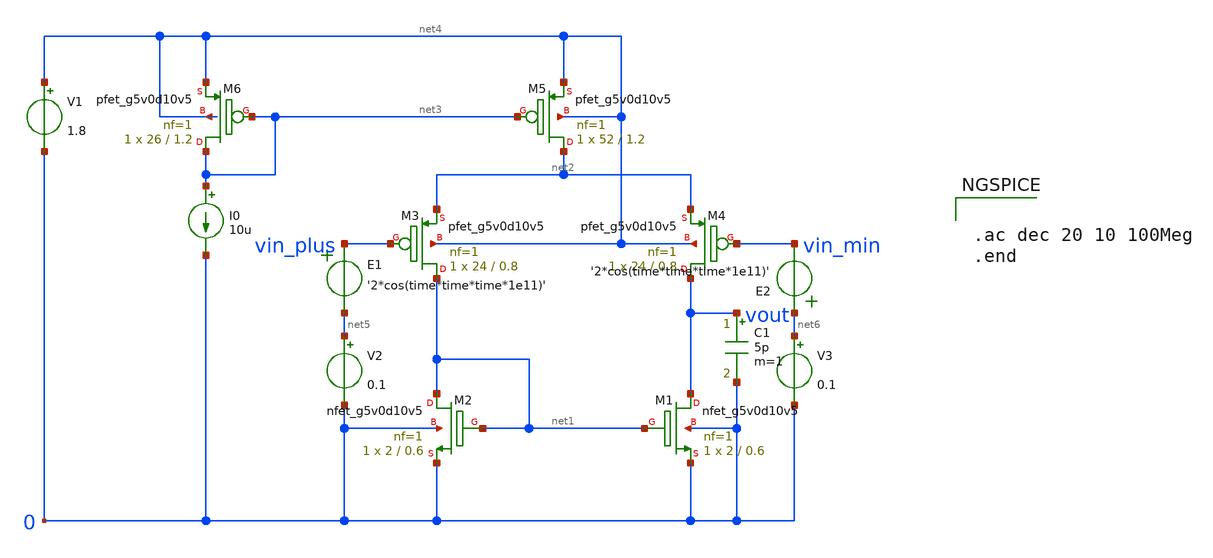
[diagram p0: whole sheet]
** sch_path: Bandgap/one_stage_opamp.sch
**.subckt one_stage_opamp
XM1 vout net1 0 0 sky130_fd_pr__nfet_g5v0d10v5 L=0.6 W=2 nf=1 ad='int((nf+1)/2) * W/nf * 0.29' as='int((nf+2)/2) * W/nf * 0.29'
+ pd='2*int((nf+1)/2) * (W/nf + 0.29)' ps='2*int((nf+2)/2) * (W/nf + 0.29)' nrd='0.29 / W' nrs='0.29 / W'
+ sa=0 sb=0 sd=0 mult=1 m=1
XM2 net1 net1 0 0 sky130_fd_pr__nfet_g5v0d10v5 L=0.6 W=2 nf=1 ad='int((nf+1)/2) * W/nf * 0.29' as='int((nf+2)/2) * W/nf * 0.29'
+ pd='2*int((nf+1)/2) * (W/nf + 0.29)' ps='2*int((nf+2)/2) * (W/nf + 0.29)' nrd='0.29 / W' nrs='0.29 / W'
+ sa=0 sb=0 sd=0 mult=1 m=1
XM3 net1 vin_plus net2 net4 sky130_fd_pr__pfet_g5v0d10v5 L=0.8 W=24 nf=1 ad='int((nf+1)/2) * W/nf * 0.29'
+ as='int((nf+2)/2) * W/nf * 0.29' pd='2*int((nf+1)/2) * (W/nf + 0.29)' ps='2*int((nf+2)/2) * (W/nf + 0.29)'
+ nrd='0.29 / W' nrs='0.29 / W' sa=0 sb=0 sd=0 mult=1 m=1
XM4 vout vin_min net2 net4 sky130_fd_pr__pfet_g5v0d10v5 L=0.8 W=24 nf=1 ad='int((nf+1)/2) * W/nf * 0.29'
+ as='int((nf+2)/2) * W/nf * 0.29' pd='2*int((nf+1)/2) * (W/nf + 0.29)' ps='2*int((nf+2)/2) * (W/nf + 0.29)'
+ nrd='0.29 / W' nrs='0.29 / W' sa=0 sb=0 sd=0 mult=1 m=1
XM5 net2 net3 net4 net4 sky130_fd_pr__pfet_g5v0d10v5 L=1.2 W=52 nf=1 ad='int((nf+1)/2) * W/nf * 0.29'
+ as='int((nf+2)/2) * W/nf * 0.29' pd='2*int((nf+1)/2) * (W/nf + 0.29)' ps='2*int((nf+2)/2) * (W/nf + 0.29)'
+ nrd='0.29 / W' nrs='0.29 / W' sa=0 sb=0 sd=0 mult=1 m=1
XM6 net3 net3 net4 net4 sky130_fd_pr__pfet_g5v0d10v5 L=1.2 W=26 nf=1 ad='int((nf+1)/2) * W/nf * 0.29'
+ as='int((nf+2)/2) * W/nf * 0.29' pd='2*int((nf+1)/2) * (W/nf + 0.29)' ps='2*int((nf+2)/2) * (W/nf + 0.29)'
+ nrd='0.29 / W' nrs='0.29 / W' sa=0 sb=0 sd=0 mult=1 m=1
I0 net3 0 10u
V1 net4 0 1.8
E1 vin_plus net5 VOL=' '2*cos(time*time*time*1e11)' '
E2 net6 vin_min VOL=' '2*cos(time*time*time*1e11)' '
C1 vout 0 5p m=1
V2 net5 0 0.1
V3 net6 0 0.1
**** begin user architecture code


.ac dec 20 10 100Meg
.end



.include $::SKYWATER_MODELS/cells/nfet_01v8/sky130_fd_pr__nfet_01v8__tt.corner.spice
.include $::SKYWATER_MODELS/cells/nfet_01v8_lvt/sky130_fd_pr__nfet_01v8_lvt__tt.corner.spice
.include $::SKYWATER_MODELS/cells/pfet_01v8/sky130_fd_pr__pfet_01v8__tt.corner.spice
.include $::SKYWATER_MODELS/cells/nfet_03v3_nvt/sky130_fd_pr__nfet_03v3_nvt__tt.corner.spice
.include $::SKYWATER_MODELS/cells/nfet_05v0_nvt/sky130_fd_pr__nfet_05v0_nvt__tt.corner.spice
.include $::SKYWATER_MODELS/cells/esd_nfet_01v8/sky130_fd_pr__esd_nfet_01v8__tt.corner.spice
.include $::SKYWATER_MODELS/cells/pfet_01v8_lvt/sky130_fd_pr__pfet_01v8_lvt__tt.corner.spice
.include $::SKYWATER_MODELS/cells/pfet_01v8_hvt/sky130_fd_pr__pfet_01v8_hvt__tt.corner.spice
.include $::SKYWATER_MODELS/cells/esd_pfet_g5v0d10v5/sky130_fd_pr__esd_pfet_g5v0d10v5__tt.corner.spice
.include $::SKYWATER_MODELS/cells/pfet_g5v0d10v5/sky130_fd_pr__pfet_g5v0d10v5__tt.corner.spice
.include $::SKYWATER_MODELS/cells/pfet_g5v0d16v0/sky130_fd_pr__pfet_g5v0d16v0__tt.corner.spice
.include $::SKYWATER_MODELS/cells/nfet_g5v0d10v5/sky130_fd_pr__nfet_g5v0d10v5__tt.corner.spice
.include $::SKYWATER_MODELS/cells/nfet_g5v0d16v0/sky130_fd_pr__nfet_g5v0d16v0__tt_discrete.corner.spice
.include $::SKYWATER_MODELS/cells/esd_nfet_g5v0d10v5/sky130_fd_pr__esd_nfet_g5v0d10v5__tt.corner.spice
.include $::SKYWATER_MODELS/models/corners/tt/nonfet.spice
* Mismatch parameters
.include $::SKYWATER_MODELS/cells/nfet_01v8/sky130_fd_pr__nfet_01v8__mismatch.corner.spice
.include $::SKYWATER_MODELS/cells/pfet_01v8/sky130_fd_pr__pfet_01v8__mismatch.corner.spice
.include $::SKYWATER_MODELS/cells/nfet_01v8_lvt/sky130_fd_pr__nfet_01v8_lvt__mismatch.corner.spice
.include $::SKYWATER_MODELS/cells/pfet_01v8_lvt/sky130_fd_pr__pfet_01v8_lvt__mismatch.corner.spice
.include $::SKYWATER_MODELS/cells/pfet_01v8_hvt/sky130_fd_pr__pfet_01v8_hvt__mismatch.corner.spice
.include $::SKYWATER_MODELS/cells/nfet_g5v0d10v5/sky130_fd_pr__nfet_g5v0d10v5__mismatch.corner.spice
.include $::SKYWATER_MODELS/cells/pfet_g5v0d10v5/sky130_fd_pr__pfet_g5v0d10v5__mismatch.corner.spice
.include $::SKYWATER_MODELS/cells/nfet_05v0_nvt/sky130_fd_pr__nfet_05v0_nvt__mismatch.corner.spice
.include $::SKYWATER_MODELS/cells/nfet_03v3_nvt/sky130_fd_pr__nfet_03v3_nvt__mismatch.corner.spice
* Resistor$::SKYWATER_MODELS/Capacitor
.include $::SKYWATER_MODELS/models/r+c/res_typical__cap_typical.spice
.include $::SKYWATER_MODELS/models/r+c/res_typical__cap_typical__lin.spice
* Special cells
.include $::SKYWATER_MODELS/models/corners/tt/specialized_cells.spice
* All models
.include $::SKYWATER_MODELS/models/all.spice
* Corner
.include $::SKYWATER_MODELS/models/corners/tt/rf.spice

**** end user architecture code
**.ends
.end
